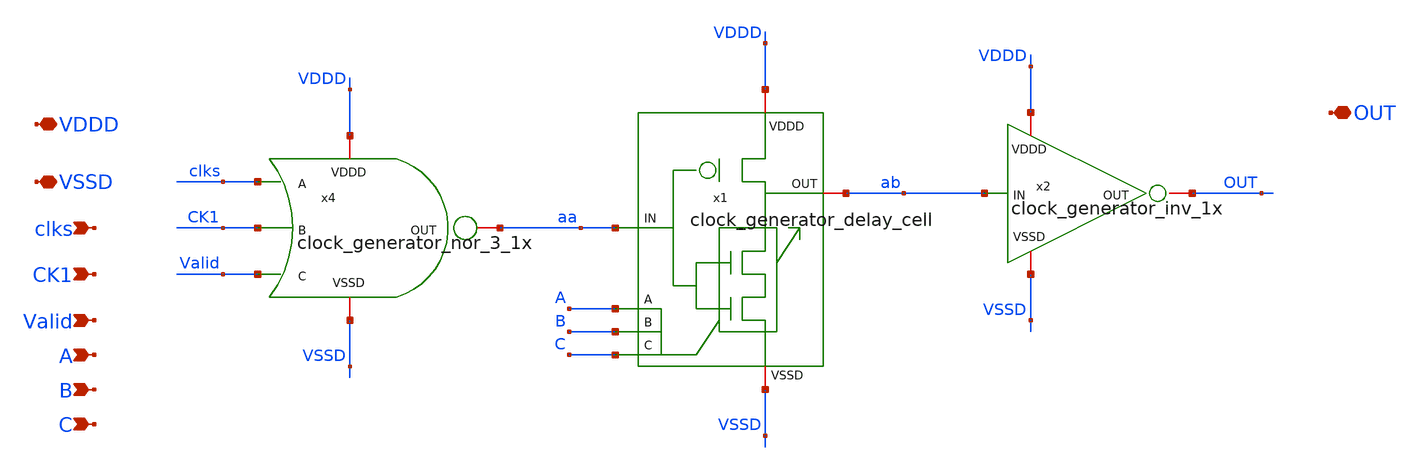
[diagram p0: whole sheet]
** sch_path: SAR_ADC/SAR_clock/xschem/clock_generator.sch
**.subckt clock_generator VDDD VSSD OUT clks CK1 Valid A B C
*.iopin VDDD
*.iopin VSSD
*.iopin OUT
*.ipin clks
*.ipin CK1
*.ipin Valid
*.ipin A
*.ipin B
*.ipin C
x4 VDDD aa VSSD clks CK1 Valid clock_generator_nor_3_1x
x1 VDDD VSSD ab aa A B C clock_generator_delay_cell
x2 VDDD OUT VSSD ab clock_generator_inv_1x
**.ends
.end
